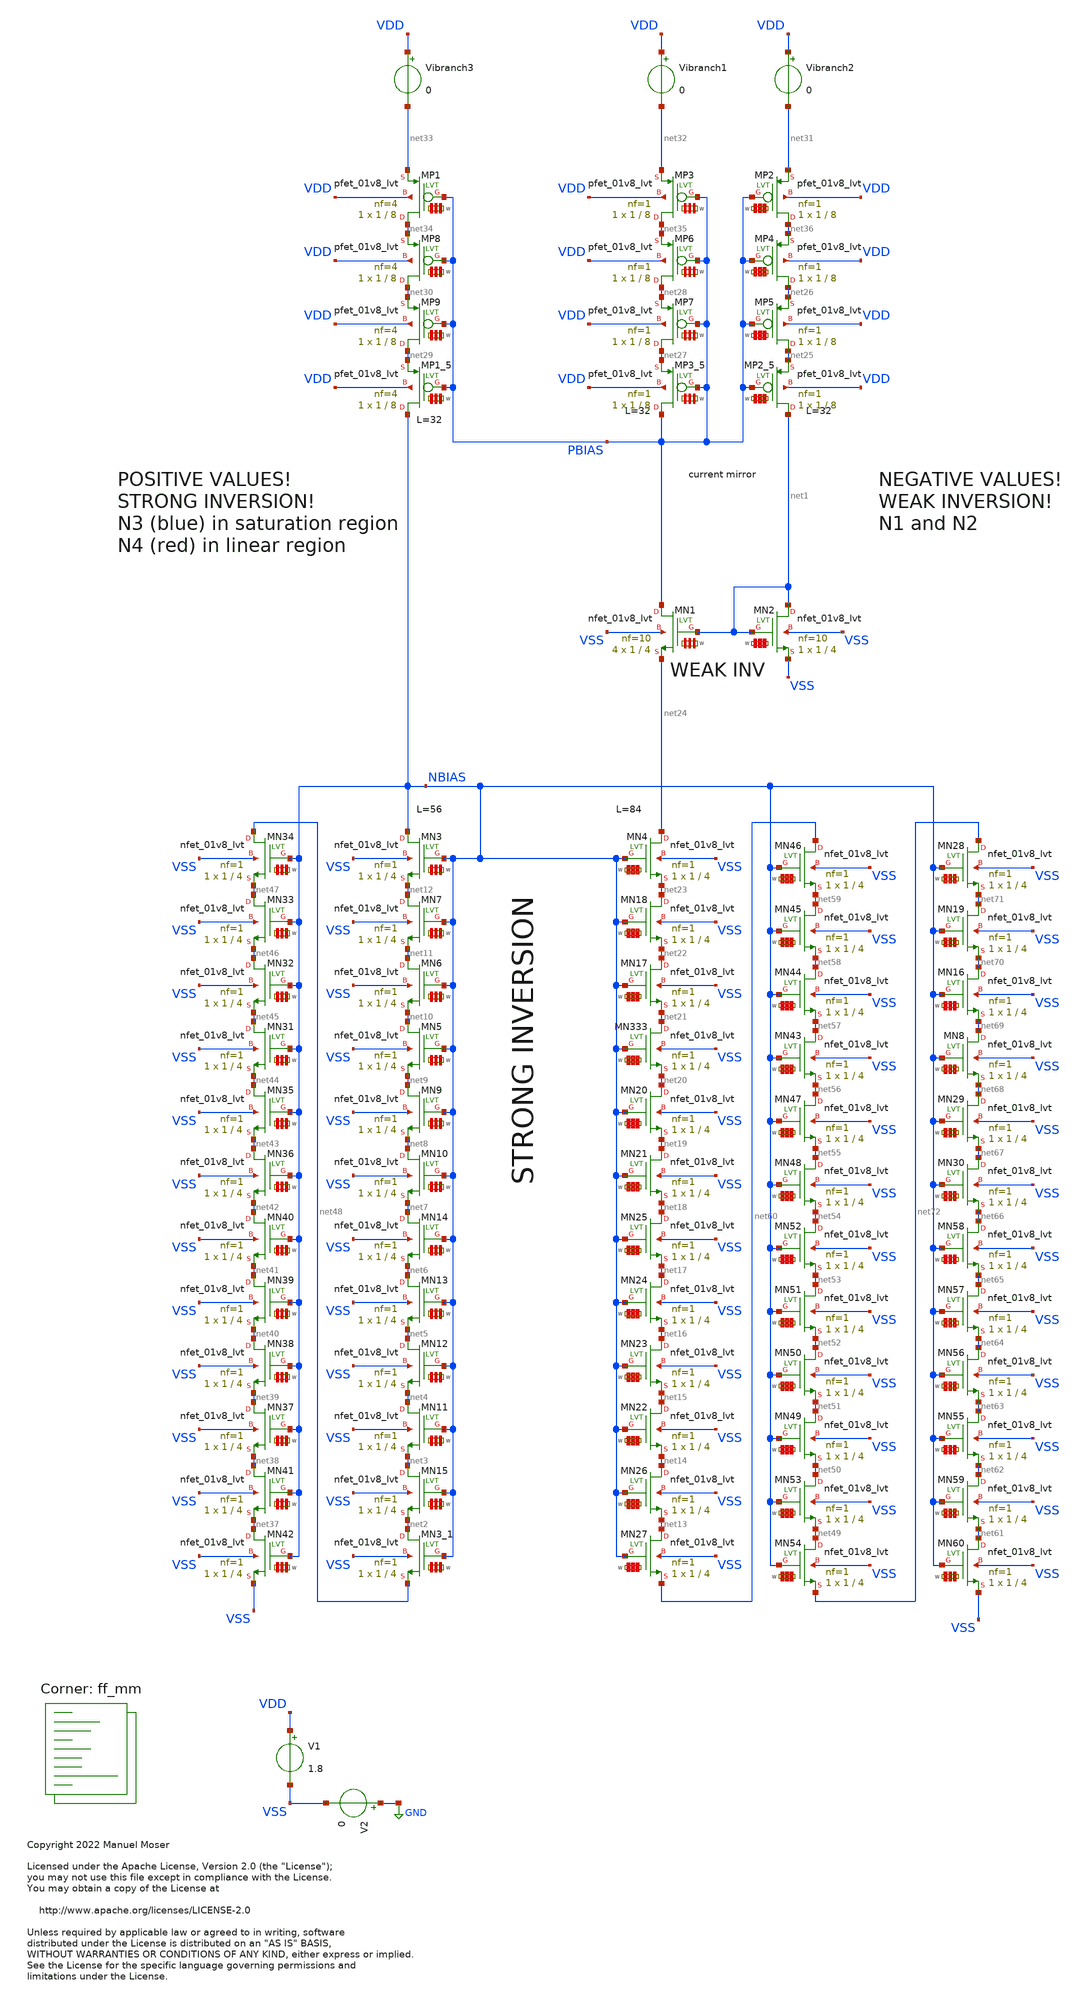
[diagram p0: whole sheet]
** sch_path: xschem/archive/const_curr_source_tb_dimensioning.sch
* Copyright 2022 Manuel Moser
* Licensed under the Apache License, Version 2.0 (the "License");
**.subckt const_curr_source_tb_dimensioning
V1 VDD VSS 1.8
V2 GND VSS 0
Vibranch1 VDD net32 0
Vibranch2 VDD net31 0
Vibranch3 VDD net33 0
XMP2 net36 PBIAS net31 VDD sky130_fd_pr__pfet_01v8_lvt L=8 W='1 * 1 ' nf=1 ad='int((nf+1)/2) * W / nf * 0.29'
+ as='int((nf+2)/2) * W / nf * 0.29' pd='2*int((nf+1)/2) * (W / nf + 0.29)' ps='2*int((nf+2)/2) * (W / nf + 0.29)'
+ nrd='0.29 / W ' nrs='0.29 / W ' sa=0 sb=0 sd=0 mult=1 m=1
XMP2_5 net1 PBIAS net25 VDD sky130_fd_pr__pfet_01v8_lvt L=8 W='1 * 1 ' nf=1 ad='int((nf+1)/2) * W / nf * 0.29'
+ as='int((nf+2)/2) * W / nf * 0.29' pd='2*int((nf+1)/2) * (W / nf + 0.29)' ps='2*int((nf+2)/2) * (W / nf + 0.29)'
+ nrd='0.29 / W ' nrs='0.29 / W ' sa=0 sb=0 sd=0 mult=1 m=1
XMP3 net35 PBIAS net32 VDD sky130_fd_pr__pfet_01v8_lvt L=8 W='1 * 1 ' nf=1 ad='int((nf+1)/2) * W / nf * 0.29'
+ as='int((nf+2)/2) * W / nf * 0.29' pd='2*int((nf+1)/2) * (W / nf + 0.29)' ps='2*int((nf+2)/2) * (W / nf + 0.29)'
+ nrd='0.29 / W ' nrs='0.29 / W ' sa=0 sb=0 sd=0 mult=1 m=1
XMP3_5 PBIAS PBIAS net27 VDD sky130_fd_pr__pfet_01v8_lvt L=8 W='1 * 1 ' nf=1 ad='int((nf+1)/2) * W / nf * 0.29'
+ as='int((nf+2)/2) * W / nf * 0.29' pd='2*int((nf+1)/2) * (W / nf + 0.29)' ps='2*int((nf+2)/2) * (W / nf + 0.29)'
+ nrd='0.29 / W ' nrs='0.29 / W ' sa=0 sb=0 sd=0 mult=1 m=1
XMP1 net34 PBIAS net33 VDD sky130_fd_pr__pfet_01v8_lvt L=8 W='1 * 4 ' nf=4 ad='int((nf+1)/2) * W / nf * 0.29'
+ as='int((nf+2)/2) * W / nf * 0.29' pd='2*int((nf+1)/2) * (W / nf + 0.29)' ps='2*int((nf+2)/2) * (W / nf + 0.29)'
+ nrd='0.29 / W ' nrs='0.29 / W ' sa=0 sb=0 sd=0 mult=1 m=1
XMP1_5 NBIAS PBIAS net29 VDD sky130_fd_pr__pfet_01v8_lvt L=8 W='1 * 4 ' nf=4 ad='int((nf+1)/2) * W / nf * 0.29'
+ as='int((nf+2)/2) * W / nf * 0.29' pd='2*int((nf+1)/2) * (W / nf + 0.29)' ps='2*int((nf+2)/2) * (W / nf + 0.29)'
+ nrd='0.29 / W ' nrs='0.29 / W ' sa=0 sb=0 sd=0 mult=1 m=1
XMN5 net10 NBIAS net9 VSS sky130_fd_pr__nfet_01v8_lvt L=4 W='1 * 1 ' nf=1 ad='int((nf+1)/2) * W / nf * 0.29'
+ as='int((nf+2)/2) * W / nf * 0.29' pd='2*int((nf+1)/2) * (W / nf + 0.29)' ps='2*int((nf+2)/2) * (W / nf + 0.29)'
+ nrd='0.29 / W ' nrs='0.29 / W ' sa=0 sb=0 sd=0 mult=1 m=1
XMN6 net11 NBIAS net10 VSS sky130_fd_pr__nfet_01v8_lvt L=4 W='1 * 1 ' nf=1 ad='int((nf+1)/2) * W / nf * 0.29'
+ as='int((nf+2)/2) * W / nf * 0.29' pd='2*int((nf+1)/2) * (W / nf + 0.29)' ps='2*int((nf+2)/2) * (W / nf + 0.29)'
+ nrd='0.29 / W ' nrs='0.29 / W ' sa=0 sb=0 sd=0 mult=1 m=1
XMN7 net12 NBIAS net11 VSS sky130_fd_pr__nfet_01v8_lvt L=4 W='1 * 1 ' nf=1 ad='int((nf+1)/2) * W / nf * 0.29'
+ as='int((nf+2)/2) * W / nf * 0.29' pd='2*int((nf+1)/2) * (W / nf + 0.29)' ps='2*int((nf+2)/2) * (W / nf + 0.29)'
+ nrd='0.29 / W ' nrs='0.29 / W ' sa=0 sb=0 sd=0 mult=1 m=1
XMN3 NBIAS NBIAS net12 VSS sky130_fd_pr__nfet_01v8_lvt L=4 W='1 * 1 ' nf=1 ad='int((nf+1)/2) * W / nf * 0.29'
+ as='int((nf+2)/2) * W / nf * 0.29' pd='2*int((nf+1)/2) * (W / nf + 0.29)' ps='2*int((nf+2)/2) * (W / nf + 0.29)'
+ nrd='0.29 / W ' nrs='0.29 / W ' sa=0 sb=0 sd=0 mult=1 m=1
XMN9 net9 NBIAS net8 VSS sky130_fd_pr__nfet_01v8_lvt L=4 W='1 * 1 ' nf=1 ad='int((nf+1)/2) * W / nf * 0.29'
+ as='int((nf+2)/2) * W / nf * 0.29' pd='2*int((nf+1)/2) * (W / nf + 0.29)' ps='2*int((nf+2)/2) * (W / nf + 0.29)'
+ nrd='0.29 / W ' nrs='0.29 / W ' sa=0 sb=0 sd=0 mult=1 m=1
XMN10 net8 NBIAS net7 VSS sky130_fd_pr__nfet_01v8_lvt L=4 W='1 * 1 ' nf=1 ad='int((nf+1)/2) * W / nf * 0.29'
+ as='int((nf+2)/2) * W / nf * 0.29' pd='2*int((nf+1)/2) * (W / nf + 0.29)' ps='2*int((nf+2)/2) * (W / nf + 0.29)'
+ nrd='0.29 / W ' nrs='0.29 / W ' sa=0 sb=0 sd=0 mult=1 m=1
XMN11 net4 NBIAS net3 VSS sky130_fd_pr__nfet_01v8_lvt L=4 W='1 * 1 ' nf=1 ad='int((nf+1)/2) * W / nf * 0.29'
+ as='int((nf+2)/2) * W / nf * 0.29' pd='2*int((nf+1)/2) * (W / nf + 0.29)' ps='2*int((nf+2)/2) * (W / nf + 0.29)'
+ nrd='0.29 / W ' nrs='0.29 / W ' sa=0 sb=0 sd=0 mult=1 m=1
XMN12 net5 NBIAS net4 VSS sky130_fd_pr__nfet_01v8_lvt L=4 W='1 * 1 ' nf=1 ad='int((nf+1)/2) * W / nf * 0.29'
+ as='int((nf+2)/2) * W / nf * 0.29' pd='2*int((nf+1)/2) * (W / nf + 0.29)' ps='2*int((nf+2)/2) * (W / nf + 0.29)'
+ nrd='0.29 / W ' nrs='0.29 / W ' sa=0 sb=0 sd=0 mult=1 m=1
XMN13 net6 NBIAS net5 VSS sky130_fd_pr__nfet_01v8_lvt L=4 W='1 * 1 ' nf=1 ad='int((nf+1)/2) * W / nf * 0.29'
+ as='int((nf+2)/2) * W / nf * 0.29' pd='2*int((nf+1)/2) * (W / nf + 0.29)' ps='2*int((nf+2)/2) * (W / nf + 0.29)'
+ nrd='0.29 / W ' nrs='0.29 / W ' sa=0 sb=0 sd=0 mult=1 m=1
XMN14 net7 NBIAS net6 VSS sky130_fd_pr__nfet_01v8_lvt L=4 W='1 * 1 ' nf=1 ad='int((nf+1)/2) * W / nf * 0.29'
+ as='int((nf+2)/2) * W / nf * 0.29' pd='2*int((nf+1)/2) * (W / nf + 0.29)' ps='2*int((nf+2)/2) * (W / nf + 0.29)'
+ nrd='0.29 / W ' nrs='0.29 / W ' sa=0 sb=0 sd=0 mult=1 m=1
XMN15 net3 NBIAS net2 VSS sky130_fd_pr__nfet_01v8_lvt L=4 W='1 * 1 ' nf=1 ad='int((nf+1)/2) * W / nf * 0.29'
+ as='int((nf+2)/2) * W / nf * 0.29' pd='2*int((nf+1)/2) * (W / nf + 0.29)' ps='2*int((nf+2)/2) * (W / nf + 0.29)'
+ nrd='0.29 / W ' nrs='0.29 / W ' sa=0 sb=0 sd=0 mult=1 m=1
XMN3_1 net2 NBIAS net48 VSS sky130_fd_pr__nfet_01v8_lvt L=4 W='1 * 1 ' nf=1 ad='int((nf+1)/2) * W / nf * 0.29'
+ as='int((nf+2)/2) * W / nf * 0.29' pd='2*int((nf+1)/2) * (W / nf + 0.29)' ps='2*int((nf+2)/2) * (W / nf + 0.29)'
+ nrd='0.29 / W ' nrs='0.29 / W ' sa=0 sb=0 sd=0 mult=1 m=1
XMN333 net21 NBIAS net20 VSS sky130_fd_pr__nfet_01v8_lvt L=4 W='1 * 1 ' nf=1 ad='int((nf+1)/2) * W / nf * 0.29'
+ as='int((nf+2)/2) * W / nf * 0.29' pd='2*int((nf+1)/2) * (W / nf + 0.29)' ps='2*int((nf+2)/2) * (W / nf + 0.29)'
+ nrd='0.29 / W ' nrs='0.29 / W ' sa=0 sb=0 sd=0 mult=1 m=1
XMN17 net22 NBIAS net21 VSS sky130_fd_pr__nfet_01v8_lvt L=4 W='1 * 1 ' nf=1 ad='int((nf+1)/2) * W / nf * 0.29'
+ as='int((nf+2)/2) * W / nf * 0.29' pd='2*int((nf+1)/2) * (W / nf + 0.29)' ps='2*int((nf+2)/2) * (W / nf + 0.29)'
+ nrd='0.29 / W ' nrs='0.29 / W ' sa=0 sb=0 sd=0 mult=1 m=1
XMN18 net23 NBIAS net22 VSS sky130_fd_pr__nfet_01v8_lvt L=4 W='1 * 1 ' nf=1 ad='int((nf+1)/2) * W / nf * 0.29'
+ as='int((nf+2)/2) * W / nf * 0.29' pd='2*int((nf+1)/2) * (W / nf + 0.29)' ps='2*int((nf+2)/2) * (W / nf + 0.29)'
+ nrd='0.29 / W ' nrs='0.29 / W ' sa=0 sb=0 sd=0 mult=1 m=1
XMN4 net24 NBIAS net23 VSS sky130_fd_pr__nfet_01v8_lvt L=4 W='1 * 1 ' nf=1 ad='int((nf+1)/2) * W / nf * 0.29'
+ as='int((nf+2)/2) * W / nf * 0.29' pd='2*int((nf+1)/2) * (W / nf + 0.29)' ps='2*int((nf+2)/2) * (W / nf + 0.29)'
+ nrd='0.29 / W ' nrs='0.29 / W ' sa=0 sb=0 sd=0 mult=1 m=1
XMN20 net20 NBIAS net19 VSS sky130_fd_pr__nfet_01v8_lvt L=4 W='1 * 1 ' nf=1 ad='int((nf+1)/2) * W / nf * 0.29'
+ as='int((nf+2)/2) * W / nf * 0.29' pd='2*int((nf+1)/2) * (W / nf + 0.29)' ps='2*int((nf+2)/2) * (W / nf + 0.29)'
+ nrd='0.29 / W ' nrs='0.29 / W ' sa=0 sb=0 sd=0 mult=1 m=1
XMN21 net19 NBIAS net18 VSS sky130_fd_pr__nfet_01v8_lvt L=4 W='1 * 1 ' nf=1 ad='int((nf+1)/2) * W / nf * 0.29'
+ as='int((nf+2)/2) * W / nf * 0.29' pd='2*int((nf+1)/2) * (W / nf + 0.29)' ps='2*int((nf+2)/2) * (W / nf + 0.29)'
+ nrd='0.29 / W ' nrs='0.29 / W ' sa=0 sb=0 sd=0 mult=1 m=1
XMN22 net15 NBIAS net14 VSS sky130_fd_pr__nfet_01v8_lvt L=4 W='1 * 1 ' nf=1 ad='int((nf+1)/2) * W / nf * 0.29'
+ as='int((nf+2)/2) * W / nf * 0.29' pd='2*int((nf+1)/2) * (W / nf + 0.29)' ps='2*int((nf+2)/2) * (W / nf + 0.29)'
+ nrd='0.29 / W ' nrs='0.29 / W ' sa=0 sb=0 sd=0 mult=1 m=1
XMN23 net16 NBIAS net15 VSS sky130_fd_pr__nfet_01v8_lvt L=4 W='1 * 1 ' nf=1 ad='int((nf+1)/2) * W / nf * 0.29'
+ as='int((nf+2)/2) * W / nf * 0.29' pd='2*int((nf+1)/2) * (W / nf + 0.29)' ps='2*int((nf+2)/2) * (W / nf + 0.29)'
+ nrd='0.29 / W ' nrs='0.29 / W ' sa=0 sb=0 sd=0 mult=1 m=1
XMN24 net17 NBIAS net16 VSS sky130_fd_pr__nfet_01v8_lvt L=4 W='1 * 1 ' nf=1 ad='int((nf+1)/2) * W / nf * 0.29'
+ as='int((nf+2)/2) * W / nf * 0.29' pd='2*int((nf+1)/2) * (W / nf + 0.29)' ps='2*int((nf+2)/2) * (W / nf + 0.29)'
+ nrd='0.29 / W ' nrs='0.29 / W ' sa=0 sb=0 sd=0 mult=1 m=1
XMN25 net18 NBIAS net17 VSS sky130_fd_pr__nfet_01v8_lvt L=4 W='1 * 1 ' nf=1 ad='int((nf+1)/2) * W / nf * 0.29'
+ as='int((nf+2)/2) * W / nf * 0.29' pd='2*int((nf+1)/2) * (W / nf + 0.29)' ps='2*int((nf+2)/2) * (W / nf + 0.29)'
+ nrd='0.29 / W ' nrs='0.29 / W ' sa=0 sb=0 sd=0 mult=1 m=1
XMN26 net14 NBIAS net13 VSS sky130_fd_pr__nfet_01v8_lvt L=4 W='1 * 1 ' nf=1 ad='int((nf+1)/2) * W / nf * 0.29'
+ as='int((nf+2)/2) * W / nf * 0.29' pd='2*int((nf+1)/2) * (W / nf + 0.29)' ps='2*int((nf+2)/2) * (W / nf + 0.29)'
+ nrd='0.29 / W ' nrs='0.29 / W ' sa=0 sb=0 sd=0 mult=1 m=1
XMN27 net13 NBIAS net60 VSS sky130_fd_pr__nfet_01v8_lvt L=4 W='1 * 1 ' nf=1 ad='int((nf+1)/2) * W / nf * 0.29'
+ as='int((nf+2)/2) * W / nf * 0.29' pd='2*int((nf+1)/2) * (W / nf + 0.29)' ps='2*int((nf+2)/2) * (W / nf + 0.29)'
+ nrd='0.29 / W ' nrs='0.29 / W ' sa=0 sb=0 sd=0 mult=1 m=1
XMP4 net26 PBIAS net36 VDD sky130_fd_pr__pfet_01v8_lvt L=8 W='1 * 1 ' nf=1 ad='int((nf+1)/2) * W / nf * 0.29'
+ as='int((nf+2)/2) * W / nf * 0.29' pd='2*int((nf+1)/2) * (W / nf + 0.29)' ps='2*int((nf+2)/2) * (W / nf + 0.29)'
+ nrd='0.29 / W ' nrs='0.29 / W ' sa=0 sb=0 sd=0 mult=1 m=1
XMP5 net25 PBIAS net26 VDD sky130_fd_pr__pfet_01v8_lvt L=8 W='1 * 1 ' nf=1 ad='int((nf+1)/2) * W / nf * 0.29'
+ as='int((nf+2)/2) * W / nf * 0.29' pd='2*int((nf+1)/2) * (W / nf + 0.29)' ps='2*int((nf+2)/2) * (W / nf + 0.29)'
+ nrd='0.29 / W ' nrs='0.29 / W ' sa=0 sb=0 sd=0 mult=1 m=1
XMP6 net28 PBIAS net35 VDD sky130_fd_pr__pfet_01v8_lvt L=8 W='1 * 1 ' nf=1 ad='int((nf+1)/2) * W / nf * 0.29'
+ as='int((nf+2)/2) * W / nf * 0.29' pd='2*int((nf+1)/2) * (W / nf + 0.29)' ps='2*int((nf+2)/2) * (W / nf + 0.29)'
+ nrd='0.29 / W ' nrs='0.29 / W ' sa=0 sb=0 sd=0 mult=1 m=1
XMP7 net27 PBIAS net28 VDD sky130_fd_pr__pfet_01v8_lvt L=8 W='1 * 1 ' nf=1 ad='int((nf+1)/2) * W / nf * 0.29'
+ as='int((nf+2)/2) * W / nf * 0.29' pd='2*int((nf+1)/2) * (W / nf + 0.29)' ps='2*int((nf+2)/2) * (W / nf + 0.29)'
+ nrd='0.29 / W ' nrs='0.29 / W ' sa=0 sb=0 sd=0 mult=1 m=1
XMP8 net30 PBIAS net34 VDD sky130_fd_pr__pfet_01v8_lvt L=8 W='1 * 4 ' nf=4 ad='int((nf+1)/2) * W / nf * 0.29'
+ as='int((nf+2)/2) * W / nf * 0.29' pd='2*int((nf+1)/2) * (W / nf + 0.29)' ps='2*int((nf+2)/2) * (W / nf + 0.29)'
+ nrd='0.29 / W ' nrs='0.29 / W ' sa=0 sb=0 sd=0 mult=1 m=1
XMP9 net29 PBIAS net30 VDD sky130_fd_pr__pfet_01v8_lvt L=8 W='1 * 4 ' nf=4 ad='int((nf+1)/2) * W / nf * 0.29'
+ as='int((nf+2)/2) * W / nf * 0.29' pd='2*int((nf+1)/2) * (W / nf + 0.29)' ps='2*int((nf+2)/2) * (W / nf + 0.29)'
+ nrd='0.29 / W ' nrs='0.29 / W ' sa=0 sb=0 sd=0 mult=1 m=1
XMN31 net45 NBIAS net44 VSS sky130_fd_pr__nfet_01v8_lvt L=4 W='1 * 1 ' nf=1 ad='int((nf+1)/2) * W / nf * 0.29'
+ as='int((nf+2)/2) * W / nf * 0.29' pd='2*int((nf+1)/2) * (W / nf + 0.29)' ps='2*int((nf+2)/2) * (W / nf + 0.29)'
+ nrd='0.29 / W ' nrs='0.29 / W ' sa=0 sb=0 sd=0 mult=1 m=1
XMN32 net46 NBIAS net45 VSS sky130_fd_pr__nfet_01v8_lvt L=4 W='1 * 1 ' nf=1 ad='int((nf+1)/2) * W / nf * 0.29'
+ as='int((nf+2)/2) * W / nf * 0.29' pd='2*int((nf+1)/2) * (W / nf + 0.29)' ps='2*int((nf+2)/2) * (W / nf + 0.29)'
+ nrd='0.29 / W ' nrs='0.29 / W ' sa=0 sb=0 sd=0 mult=1 m=1
XMN33 net47 NBIAS net46 VSS sky130_fd_pr__nfet_01v8_lvt L=4 W='1 * 1 ' nf=1 ad='int((nf+1)/2) * W / nf * 0.29'
+ as='int((nf+2)/2) * W / nf * 0.29' pd='2*int((nf+1)/2) * (W / nf + 0.29)' ps='2*int((nf+2)/2) * (W / nf + 0.29)'
+ nrd='0.29 / W ' nrs='0.29 / W ' sa=0 sb=0 sd=0 mult=1 m=1
XMN34 net48 NBIAS net47 VSS sky130_fd_pr__nfet_01v8_lvt L=4 W='1 * 1 ' nf=1 ad='int((nf+1)/2) * W / nf * 0.29'
+ as='int((nf+2)/2) * W / nf * 0.29' pd='2*int((nf+1)/2) * (W / nf + 0.29)' ps='2*int((nf+2)/2) * (W / nf + 0.29)'
+ nrd='0.29 / W ' nrs='0.29 / W ' sa=0 sb=0 sd=0 mult=1 m=1
XMN35 net44 NBIAS net43 VSS sky130_fd_pr__nfet_01v8_lvt L=4 W='1 * 1 ' nf=1 ad='int((nf+1)/2) * W / nf * 0.29'
+ as='int((nf+2)/2) * W / nf * 0.29' pd='2*int((nf+1)/2) * (W / nf + 0.29)' ps='2*int((nf+2)/2) * (W / nf + 0.29)'
+ nrd='0.29 / W ' nrs='0.29 / W ' sa=0 sb=0 sd=0 mult=1 m=1
XMN36 net43 NBIAS net42 VSS sky130_fd_pr__nfet_01v8_lvt L=4 W='1 * 1 ' nf=1 ad='int((nf+1)/2) * W / nf * 0.29'
+ as='int((nf+2)/2) * W / nf * 0.29' pd='2*int((nf+1)/2) * (W / nf + 0.29)' ps='2*int((nf+2)/2) * (W / nf + 0.29)'
+ nrd='0.29 / W ' nrs='0.29 / W ' sa=0 sb=0 sd=0 mult=1 m=1
XMN37 net39 NBIAS net38 VSS sky130_fd_pr__nfet_01v8_lvt L=4 W='1 * 1 ' nf=1 ad='int((nf+1)/2) * W / nf * 0.29'
+ as='int((nf+2)/2) * W / nf * 0.29' pd='2*int((nf+1)/2) * (W / nf + 0.29)' ps='2*int((nf+2)/2) * (W / nf + 0.29)'
+ nrd='0.29 / W ' nrs='0.29 / W ' sa=0 sb=0 sd=0 mult=1 m=1
XMN38 net40 NBIAS net39 VSS sky130_fd_pr__nfet_01v8_lvt L=4 W='1 * 1 ' nf=1 ad='int((nf+1)/2) * W / nf * 0.29'
+ as='int((nf+2)/2) * W / nf * 0.29' pd='2*int((nf+1)/2) * (W / nf + 0.29)' ps='2*int((nf+2)/2) * (W / nf + 0.29)'
+ nrd='0.29 / W ' nrs='0.29 / W ' sa=0 sb=0 sd=0 mult=1 m=1
XMN39 net41 NBIAS net40 VSS sky130_fd_pr__nfet_01v8_lvt L=4 W='1 * 1 ' nf=1 ad='int((nf+1)/2) * W / nf * 0.29'
+ as='int((nf+2)/2) * W / nf * 0.29' pd='2*int((nf+1)/2) * (W / nf + 0.29)' ps='2*int((nf+2)/2) * (W / nf + 0.29)'
+ nrd='0.29 / W ' nrs='0.29 / W ' sa=0 sb=0 sd=0 mult=1 m=1
XMN40 net42 NBIAS net41 VSS sky130_fd_pr__nfet_01v8_lvt L=4 W='1 * 1 ' nf=1 ad='int((nf+1)/2) * W / nf * 0.29'
+ as='int((nf+2)/2) * W / nf * 0.29' pd='2*int((nf+1)/2) * (W / nf + 0.29)' ps='2*int((nf+2)/2) * (W / nf + 0.29)'
+ nrd='0.29 / W ' nrs='0.29 / W ' sa=0 sb=0 sd=0 mult=1 m=1
XMN41 net38 NBIAS net37 VSS sky130_fd_pr__nfet_01v8_lvt L=4 W='1 * 1 ' nf=1 ad='int((nf+1)/2) * W / nf * 0.29'
+ as='int((nf+2)/2) * W / nf * 0.29' pd='2*int((nf+1)/2) * (W / nf + 0.29)' ps='2*int((nf+2)/2) * (W / nf + 0.29)'
+ nrd='0.29 / W ' nrs='0.29 / W ' sa=0 sb=0 sd=0 mult=1 m=1
XMN42 net37 NBIAS VSS VSS sky130_fd_pr__nfet_01v8_lvt L=4 W='1 * 1 ' nf=1 ad='int((nf+1)/2) * W / nf * 0.29'
+ as='int((nf+2)/2) * W / nf * 0.29' pd='2*int((nf+1)/2) * (W / nf + 0.29)' ps='2*int((nf+2)/2) * (W / nf + 0.29)'
+ nrd='0.29 / W ' nrs='0.29 / W ' sa=0 sb=0 sd=0 mult=1 m=1
XMN43 net57 NBIAS net56 VSS sky130_fd_pr__nfet_01v8_lvt L=4 W='1 * 1 ' nf=1 ad='int((nf+1)/2) * W / nf * 0.29'
+ as='int((nf+2)/2) * W / nf * 0.29' pd='2*int((nf+1)/2) * (W / nf + 0.29)' ps='2*int((nf+2)/2) * (W / nf + 0.29)'
+ nrd='0.29 / W ' nrs='0.29 / W ' sa=0 sb=0 sd=0 mult=1 m=1
XMN44 net58 NBIAS net57 VSS sky130_fd_pr__nfet_01v8_lvt L=4 W='1 * 1 ' nf=1 ad='int((nf+1)/2) * W / nf * 0.29'
+ as='int((nf+2)/2) * W / nf * 0.29' pd='2*int((nf+1)/2) * (W / nf + 0.29)' ps='2*int((nf+2)/2) * (W / nf + 0.29)'
+ nrd='0.29 / W ' nrs='0.29 / W ' sa=0 sb=0 sd=0 mult=1 m=1
XMN45 net59 NBIAS net58 VSS sky130_fd_pr__nfet_01v8_lvt L=4 W='1 * 1 ' nf=1 ad='int((nf+1)/2) * W / nf * 0.29'
+ as='int((nf+2)/2) * W / nf * 0.29' pd='2*int((nf+1)/2) * (W / nf + 0.29)' ps='2*int((nf+2)/2) * (W / nf + 0.29)'
+ nrd='0.29 / W ' nrs='0.29 / W ' sa=0 sb=0 sd=0 mult=1 m=1
XMN46 net60 NBIAS net59 VSS sky130_fd_pr__nfet_01v8_lvt L=4 W='1 * 1 ' nf=1 ad='int((nf+1)/2) * W / nf * 0.29'
+ as='int((nf+2)/2) * W / nf * 0.29' pd='2*int((nf+1)/2) * (W / nf + 0.29)' ps='2*int((nf+2)/2) * (W / nf + 0.29)'
+ nrd='0.29 / W ' nrs='0.29 / W ' sa=0 sb=0 sd=0 mult=1 m=1
XMN47 net56 NBIAS net55 VSS sky130_fd_pr__nfet_01v8_lvt L=4 W='1 * 1 ' nf=1 ad='int((nf+1)/2) * W / nf * 0.29'
+ as='int((nf+2)/2) * W / nf * 0.29' pd='2*int((nf+1)/2) * (W / nf + 0.29)' ps='2*int((nf+2)/2) * (W / nf + 0.29)'
+ nrd='0.29 / W ' nrs='0.29 / W ' sa=0 sb=0 sd=0 mult=1 m=1
XMN48 net55 NBIAS net54 VSS sky130_fd_pr__nfet_01v8_lvt L=4 W='1 * 1 ' nf=1 ad='int((nf+1)/2) * W / nf * 0.29'
+ as='int((nf+2)/2) * W / nf * 0.29' pd='2*int((nf+1)/2) * (W / nf + 0.29)' ps='2*int((nf+2)/2) * (W / nf + 0.29)'
+ nrd='0.29 / W ' nrs='0.29 / W ' sa=0 sb=0 sd=0 mult=1 m=1
XMN49 net51 NBIAS net50 VSS sky130_fd_pr__nfet_01v8_lvt L=4 W='1 * 1 ' nf=1 ad='int((nf+1)/2) * W / nf * 0.29'
+ as='int((nf+2)/2) * W / nf * 0.29' pd='2*int((nf+1)/2) * (W / nf + 0.29)' ps='2*int((nf+2)/2) * (W / nf + 0.29)'
+ nrd='0.29 / W ' nrs='0.29 / W ' sa=0 sb=0 sd=0 mult=1 m=1
XMN50 net52 NBIAS net51 VSS sky130_fd_pr__nfet_01v8_lvt L=4 W='1 * 1 ' nf=1 ad='int((nf+1)/2) * W / nf * 0.29'
+ as='int((nf+2)/2) * W / nf * 0.29' pd='2*int((nf+1)/2) * (W / nf + 0.29)' ps='2*int((nf+2)/2) * (W / nf + 0.29)'
+ nrd='0.29 / W ' nrs='0.29 / W ' sa=0 sb=0 sd=0 mult=1 m=1
XMN51 net53 NBIAS net52 VSS sky130_fd_pr__nfet_01v8_lvt L=4 W='1 * 1 ' nf=1 ad='int((nf+1)/2) * W / nf * 0.29'
+ as='int((nf+2)/2) * W / nf * 0.29' pd='2*int((nf+1)/2) * (W / nf + 0.29)' ps='2*int((nf+2)/2) * (W / nf + 0.29)'
+ nrd='0.29 / W ' nrs='0.29 / W ' sa=0 sb=0 sd=0 mult=1 m=1
XMN52 net54 NBIAS net53 VSS sky130_fd_pr__nfet_01v8_lvt L=4 W='1 * 1 ' nf=1 ad='int((nf+1)/2) * W / nf * 0.29'
+ as='int((nf+2)/2) * W / nf * 0.29' pd='2*int((nf+1)/2) * (W / nf + 0.29)' ps='2*int((nf+2)/2) * (W / nf + 0.29)'
+ nrd='0.29 / W ' nrs='0.29 / W ' sa=0 sb=0 sd=0 mult=1 m=1
XMN53 net50 NBIAS net49 VSS sky130_fd_pr__nfet_01v8_lvt L=4 W='1 * 1 ' nf=1 ad='int((nf+1)/2) * W / nf * 0.29'
+ as='int((nf+2)/2) * W / nf * 0.29' pd='2*int((nf+1)/2) * (W / nf + 0.29)' ps='2*int((nf+2)/2) * (W / nf + 0.29)'
+ nrd='0.29 / W ' nrs='0.29 / W ' sa=0 sb=0 sd=0 mult=1 m=1
XMN54 net49 NBIAS net72 VSS sky130_fd_pr__nfet_01v8_lvt L=4 W='1 * 1 ' nf=1 ad='int((nf+1)/2) * W / nf * 0.29'
+ as='int((nf+2)/2) * W / nf * 0.29' pd='2*int((nf+1)/2) * (W / nf + 0.29)' ps='2*int((nf+2)/2) * (W / nf + 0.29)'
+ nrd='0.29 / W ' nrs='0.29 / W ' sa=0 sb=0 sd=0 mult=1 m=1
XMN8 net69 NBIAS net68 VSS sky130_fd_pr__nfet_01v8_lvt L=4 W='1 * 1 ' nf=1 ad='int((nf+1)/2) * W / nf * 0.29'
+ as='int((nf+2)/2) * W / nf * 0.29' pd='2*int((nf+1)/2) * (W / nf + 0.29)' ps='2*int((nf+2)/2) * (W / nf + 0.29)'
+ nrd='0.29 / W ' nrs='0.29 / W ' sa=0 sb=0 sd=0 mult=1 m=1
XMN16 net70 NBIAS net69 VSS sky130_fd_pr__nfet_01v8_lvt L=4 W='1 * 1 ' nf=1 ad='int((nf+1)/2) * W / nf * 0.29'
+ as='int((nf+2)/2) * W / nf * 0.29' pd='2*int((nf+1)/2) * (W / nf + 0.29)' ps='2*int((nf+2)/2) * (W / nf + 0.29)'
+ nrd='0.29 / W ' nrs='0.29 / W ' sa=0 sb=0 sd=0 mult=1 m=1
XMN19 net71 NBIAS net70 VSS sky130_fd_pr__nfet_01v8_lvt L=4 W='1 * 1 ' nf=1 ad='int((nf+1)/2) * W / nf * 0.29'
+ as='int((nf+2)/2) * W / nf * 0.29' pd='2*int((nf+1)/2) * (W / nf + 0.29)' ps='2*int((nf+2)/2) * (W / nf + 0.29)'
+ nrd='0.29 / W ' nrs='0.29 / W ' sa=0 sb=0 sd=0 mult=1 m=1
XMN28 net72 NBIAS net71 VSS sky130_fd_pr__nfet_01v8_lvt L=4 W='1 * 1 ' nf=1 ad='int((nf+1)/2) * W / nf * 0.29'
+ as='int((nf+2)/2) * W / nf * 0.29' pd='2*int((nf+1)/2) * (W / nf + 0.29)' ps='2*int((nf+2)/2) * (W / nf + 0.29)'
+ nrd='0.29 / W ' nrs='0.29 / W ' sa=0 sb=0 sd=0 mult=1 m=1
XMN29 net68 NBIAS net67 VSS sky130_fd_pr__nfet_01v8_lvt L=4 W='1 * 1 ' nf=1 ad='int((nf+1)/2) * W / nf * 0.29'
+ as='int((nf+2)/2) * W / nf * 0.29' pd='2*int((nf+1)/2) * (W / nf + 0.29)' ps='2*int((nf+2)/2) * (W / nf + 0.29)'
+ nrd='0.29 / W ' nrs='0.29 / W ' sa=0 sb=0 sd=0 mult=1 m=1
XMN30 net67 NBIAS net66 VSS sky130_fd_pr__nfet_01v8_lvt L=4 W='1 * 1 ' nf=1 ad='int((nf+1)/2) * W / nf * 0.29'
+ as='int((nf+2)/2) * W / nf * 0.29' pd='2*int((nf+1)/2) * (W / nf + 0.29)' ps='2*int((nf+2)/2) * (W / nf + 0.29)'
+ nrd='0.29 / W ' nrs='0.29 / W ' sa=0 sb=0 sd=0 mult=1 m=1
XMN55 net63 NBIAS net62 VSS sky130_fd_pr__nfet_01v8_lvt L=4 W='1 * 1 ' nf=1 ad='int((nf+1)/2) * W / nf * 0.29'
+ as='int((nf+2)/2) * W / nf * 0.29' pd='2*int((nf+1)/2) * (W / nf + 0.29)' ps='2*int((nf+2)/2) * (W / nf + 0.29)'
+ nrd='0.29 / W ' nrs='0.29 / W ' sa=0 sb=0 sd=0 mult=1 m=1
XMN56 net64 NBIAS net63 VSS sky130_fd_pr__nfet_01v8_lvt L=4 W='1 * 1 ' nf=1 ad='int((nf+1)/2) * W / nf * 0.29'
+ as='int((nf+2)/2) * W / nf * 0.29' pd='2*int((nf+1)/2) * (W / nf + 0.29)' ps='2*int((nf+2)/2) * (W / nf + 0.29)'
+ nrd='0.29 / W ' nrs='0.29 / W ' sa=0 sb=0 sd=0 mult=1 m=1
XMN57 net65 NBIAS net64 VSS sky130_fd_pr__nfet_01v8_lvt L=4 W='1 * 1 ' nf=1 ad='int((nf+1)/2) * W / nf * 0.29'
+ as='int((nf+2)/2) * W / nf * 0.29' pd='2*int((nf+1)/2) * (W / nf + 0.29)' ps='2*int((nf+2)/2) * (W / nf + 0.29)'
+ nrd='0.29 / W ' nrs='0.29 / W ' sa=0 sb=0 sd=0 mult=1 m=1
XMN58 net66 NBIAS net65 VSS sky130_fd_pr__nfet_01v8_lvt L=4 W='1 * 1 ' nf=1 ad='int((nf+1)/2) * W / nf * 0.29'
+ as='int((nf+2)/2) * W / nf * 0.29' pd='2*int((nf+1)/2) * (W / nf + 0.29)' ps='2*int((nf+2)/2) * (W / nf + 0.29)'
+ nrd='0.29 / W ' nrs='0.29 / W ' sa=0 sb=0 sd=0 mult=1 m=1
XMN59 net62 NBIAS net61 VSS sky130_fd_pr__nfet_01v8_lvt L=4 W='1 * 1 ' nf=1 ad='int((nf+1)/2) * W / nf * 0.29'
+ as='int((nf+2)/2) * W / nf * 0.29' pd='2*int((nf+1)/2) * (W / nf + 0.29)' ps='2*int((nf+2)/2) * (W / nf + 0.29)'
+ nrd='0.29 / W ' nrs='0.29 / W ' sa=0 sb=0 sd=0 mult=1 m=1
XMN60 net61 NBIAS VSS VSS sky130_fd_pr__nfet_01v8_lvt L=4 W='1 * 1 ' nf=1 ad='int((nf+1)/2) * W / nf * 0.29'
+ as='int((nf+2)/2) * W / nf * 0.29' pd='2*int((nf+1)/2) * (W / nf + 0.29)' ps='2*int((nf+2)/2) * (W / nf + 0.29)'
+ nrd='0.29 / W ' nrs='0.29 / W ' sa=0 sb=0 sd=0 mult=1 m=1
XMN1 PBIAS net1 net24 VSS sky130_fd_pr__nfet_01v8_lvt L=4 W='1 * 10 ' nf=10 ad='int((nf+1)/2) * W / nf * 0.29'
+ as='int((nf+2)/2) * W / nf * 0.29' pd='2*int((nf+1)/2) * (W / nf + 0.29)' ps='2*int((nf+2)/2) * (W / nf + 0.29)'
+ nrd='0.29 / W ' nrs='0.29 / W ' sa=0 sb=0 sd=0 mult=4 m=4
XMN2 net1 net1 VSS VSS sky130_fd_pr__nfet_01v8_lvt L=4 W='1 * 10 ' nf=10 ad='int((nf+1)/2) * W / nf * 0.29'
+ as='int((nf+2)/2) * W / nf * 0.29' pd='2*int((nf+1)/2) * (W / nf + 0.29)' ps='2*int((nf+2)/2) * (W / nf + 0.29)'
+ nrd='0.29 / W ' nrs='0.29 / W ' sa=0 sb=0 sd=0 mult=1 m=1
**** begin user architecture code



.temp 27
.options savecurrents
.save all


* Save MN1
.save @m.xmn1.msky130_fd_pr__nfet_01v8_lvt[Vth] @m.xmn1.msky130_fd_pr__nfet_01v8_lvt[Vgs] @m.xmn1.msky130_fd_pr__nfet_01v8_lvt[Vds]

* Save MN2
.save @m.xmn2.msky130_fd_pr__nfet_01v8_lvt[Vth] @m.xmn2.msky130_fd_pr__nfet_01v8_lvt[Vgs] @m.xmn2.msky130_fd_pr__nfet_01v8_lvt[Vds]

* Save xxx
.save @m.xmn3.msky130_fd_pr__nfet_01v8_lvt[Vth] @m.xmn3.msky130_fd_pr__nfet_01v8_lvt[Vgs] @m.xmn3.msky130_fd_pr__nfet_01v8_lvt[Vds]
.save @m.xmn4.msky130_fd_pr__nfet_01v8_lvt[Vth] @m.xmn4.msky130_fd_pr__nfet_01v8_lvt[Vgs] @m.xmn4.msky130_fd_pr__nfet_01v8_lvt[Vds]
.save @m.xmp1.msky130_fd_pr__pfet_01v8_lvt[Vth]
.save @m.xmp2.msky130_fd_pr__pfet_01v8_lvt[Vth]
.save @m.xmp3.msky130_fd_pr__pfet_01v8_lvt[Vth]

.control

set num_threads = 12

write const_curr_source_tb_dimensioning.raw
set appendwrite


repeat 30
  reset
  dc V1 0.5 1.8 0.02 temp -30 60 90
  write const_curr_source_tb_dimensioning.raw i(Vibranch1) i(Vibranch2) i(Vibranch3) {(v(@m.xmn1.msky130_fd_pr__nfet_01v8_lvt[Vgs])-v(@m.xmn1.msky130_fd_pr__nfet_01v8_lvt[Vth]))}
+ {(v(@m.xmn2.msky130_fd_pr__nfet_01v8_lvt[Vgs])-v(@m.xmn2.msky130_fd_pr__nfet_01v8_lvt[Vth]))} {(v(@m.xmn3.msky130_fd_pr__nfet_01v8_lvt[Vgs])-v(@m.xmn3.msky130_fd_pr__nfet_01v8_lvt[Vth]))}
+ {(v(@m.xmn4.msky130_fd_pr__nfet_01v8_lvt[Vgs])-v(@m.xmn4.msky130_fd_pr__nfet_01v8_lvt[Vth]))}
end

* Calculate if mosfets are in the correct area
set temp = -30
op

let MN1_vov =
+ v(@m.xmn1.msky130_fd_pr__nfet_01v8_lvt[Vgs])-v(@m.xmn1.msky130_fd_pr__nfet_01v8_lvt[Vth])
let MN2_vov =
+ v(@m.xmn2.msky130_fd_pr__nfet_01v8_lvt[Vgs])-v(@m.xmn2.msky130_fd_pr__nfet_01v8_lvt[Vth])
let MN3_vov =
+ v(@m.xmn3.msky130_fd_pr__nfet_01v8_lvt[Vgs])-v(@m.xmn3.msky130_fd_pr__nfet_01v8_lvt[Vth])
let MN4_vov =
+ v(@m.xmn4.msky130_fd_pr__nfet_01v8_lvt[Vgs])-v(@m.xmn4.msky130_fd_pr__nfet_01v8_lvt[Vth])

echo MN1 and MN2 must be in weak inversion region (negative value)
print MN1_vov
print MN2_vov

echo MN3 and MN4 must be in strong inversion region (positive value)
print MN3_vov
print MN4_vov

.endc




.lib $::SKYWATER_MODELS/sky130.lib.spice ff_mm
**** end user architecture code
**.ends
.GLOBAL GND
.end
